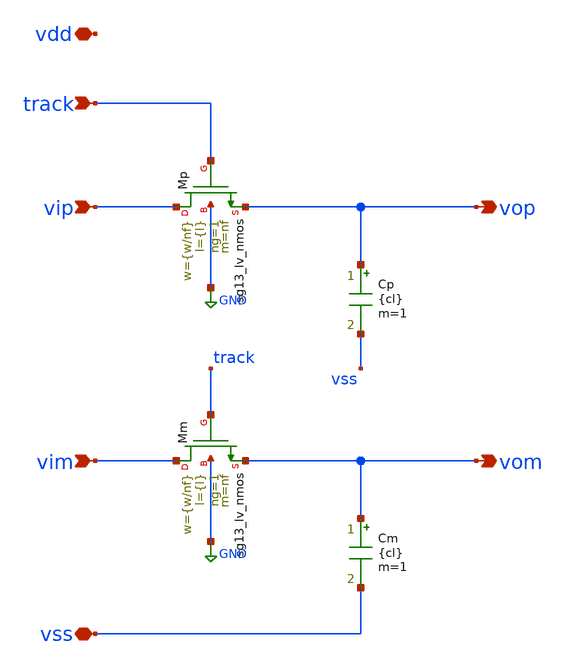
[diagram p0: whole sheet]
** sch_path: th_nmos/xschem/th_nmos.sch
**.subckt th_nmos vip vop vim vom track vss vdd
*.ipin vip
*.opin vop
*.ipin vim
*.opin vom
*.ipin track
*.iopin vss
*.iopin vdd
XMp vip track vop GND sg13_lv_nmos w={w/nf} l={l} ng=1 m=nf mm_ok=1
Cp vop vss {cl} m=1
XMm vim track vom GND sg13_lv_nmos w={w/nf} l={l} ng=1 m=nf mm_ok=1
Cm vom vss {cl} m=1
**.ends
.GLOBAL GND
.end
